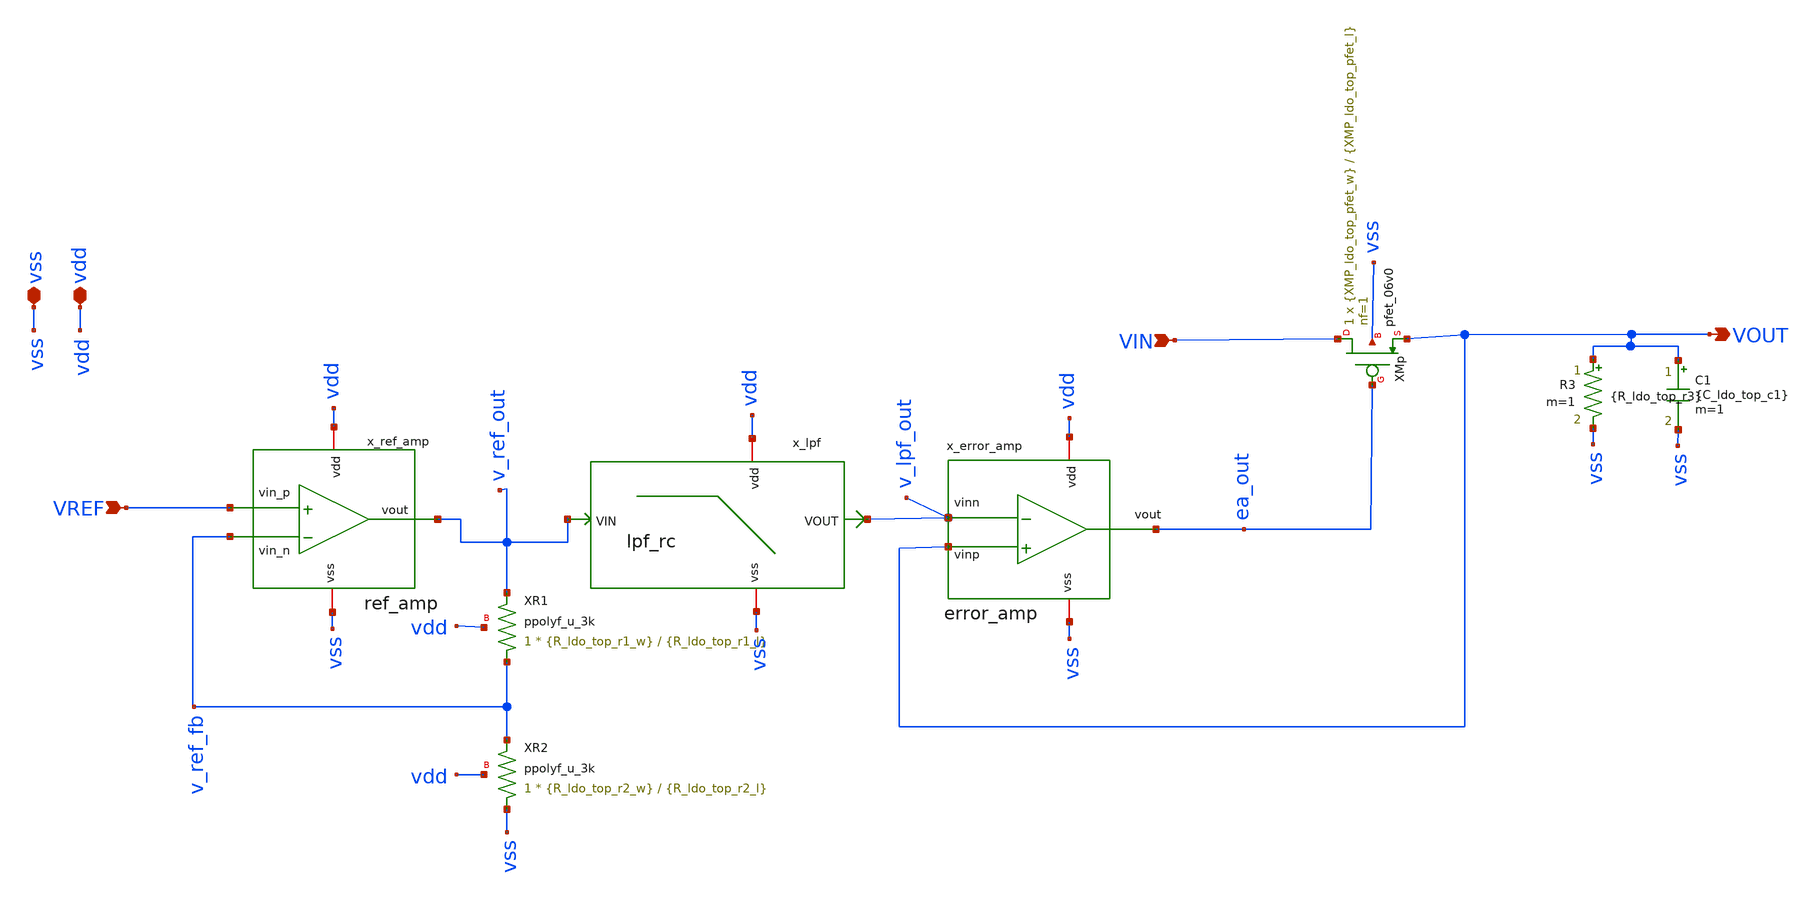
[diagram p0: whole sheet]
** sch_path: analog-db/circuits/ldo_005_buffered_ref/reference/ti-ldo/ldo/ldo.sch
**.subckt ldo VREF vdd vss VIN VOUT
*.ipin VREF
*.iopin vdd
*.iopin vss
*.ipin VIN
*.opin VOUT
x_ref_amp VREF v_ref_fb v_ref_out vdd vss ref_amp
XR1 v_ref_fb v_ref_out vdd ppolyf_u_3k r_width={R_ldo_top_r1_w} r_length={R_ldo_top_r1_l} m=1
XR2 vss v_ref_fb vdd ppolyf_u_3k r_width={R_ldo_top_r2_w} r_length={R_ldo_top_r2_l} m=1
x_error_amp vdd ea_out VOUT v_lpf_out vss error_amp
x_lpf net1 vss v_lpf_out v_ref_out lpf_rc
R3 VOUT vss {R_ldo_top_r3} m=1
C1 VOUT vss {C_ldo_top_c1} m=1
XMp VIN ea_out VOUT vss pfet_06v0 L={XMP_ldo_top_pfet_l} W={XMP_ldo_top_pfet_w} nf=1 ad='int((nf+1)/2) * W/nf * 0.18u'
+ as='int((nf+2)/2) * W/nf * 0.18u' pd='2*int((nf+1)/2) * (W/nf + 0.18u)' ps='2*int((nf+2)/2) * (W/nf + 0.18u)'
+ nrd='0.18u / W' nrs='0.18u / W' sa=0 sb=0 sd=0 m=1
**.ends
.end
